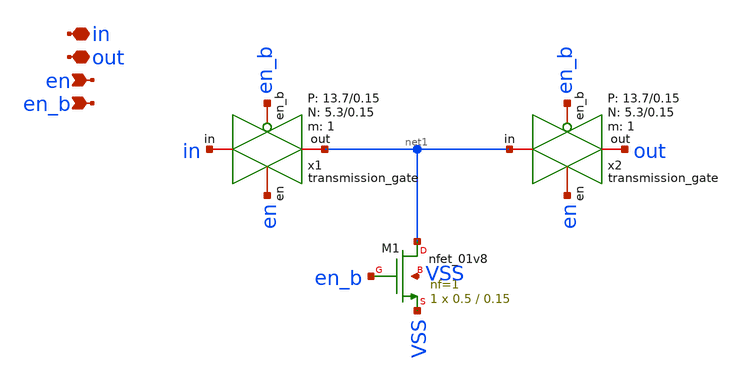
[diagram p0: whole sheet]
** sch_path: design/analog_modulator/schematic/switch_5t.sch
**.subckt switch_5t in out en en_b
*.iopin in
*.iopin out
*.ipin en
*.ipin en_b
x1 in net1 en en_b VDD VSS 1 5.3 0.15 13.7 0.15 transmission_gate
x2 net1 out en en_b VDD VSS 1 5.3 0.15 13.7 0.15 transmission_gate
XM1 net1 en_b VSS VSS sky130_fd_pr__nfet_01v8 L=0.15 W=0.5 nf=1 ad='int((nf+1)/2) * W/nf * 0.29' as='int((nf+2)/2) * W/nf * 0.29'
+ pd='2*int((nf+1)/2) * (W/nf + 0.29)' ps='2*int((nf+2)/2) * (W/nf + 0.29)' nrd='0.29 / W' nrs='0.29 / W'
+ sa=0 sb=0 sd=0 mult=1 m=1
**.ends

* expanding   symbol:  transmission_gate.sym # of pins=4
** sym_path: design/analog_modulator/schematic/transmission_gate.sym
** sch_path: design/analog_modulator/schematic/transmission_gate.sch
.subckt transmission_gate in out en en_b VDD VSS N W_N L_N W_P L_P    N=1 W_N=5.3 L_N=0.15 W_P=13.7
+ L_P=0.15
*.iopin in
*.iopin out
*.ipin en
*.ipin en_b
XM1 out en in VSS sky130_fd_pr__nfet_01v8 L='L_N' W='W_N' nf=1 ad='int((nf+1)/2) * W/nf * 0.29' as='int((nf+2)/2) * W/nf * 0.29'
+ pd='2*int((nf+1)/2) * (W/nf + 0.29)' ps='2*int((nf+2)/2) * (W/nf + 0.29)' nrd='0.29 / W' nrs='0.29 / W'
+ sa=0 sb=0 sd=0 mult='N' m='N'
XM2 out en_b in VDD sky130_fd_pr__pfet_01v8 L='L_P' W='W_P' nf=1 ad='int((nf+1)/2) * W/nf * 0.29' as='int((nf+2)/2) * W/nf * 0.29'
+ pd='2*int((nf+1)/2) * (W/nf + 0.29)' ps='2*int((nf+2)/2) * (W/nf + 0.29)' nrd='0.29 / W' nrs='0.29 / W'
+ sa=0 sb=0 sd=0 mult='N' m='N'
.ends

.end
